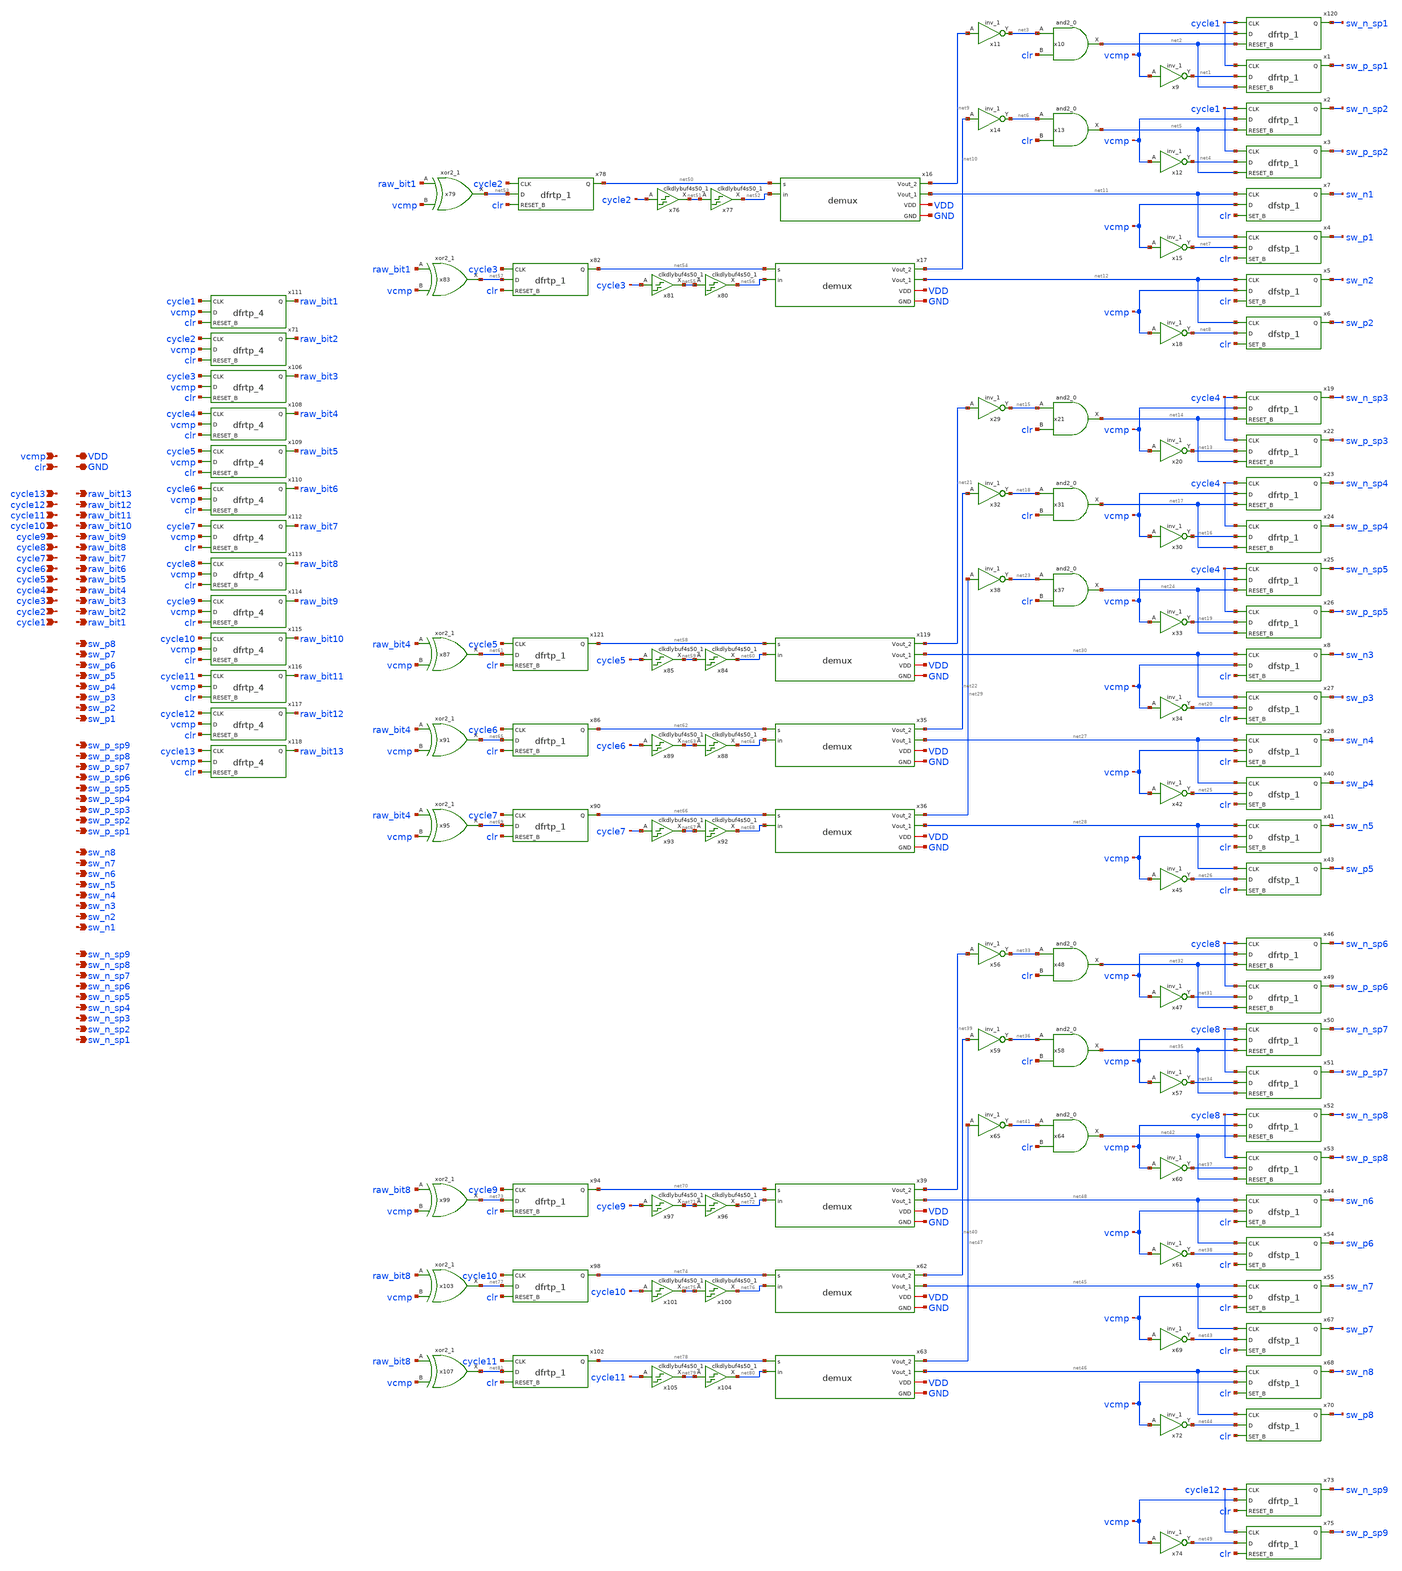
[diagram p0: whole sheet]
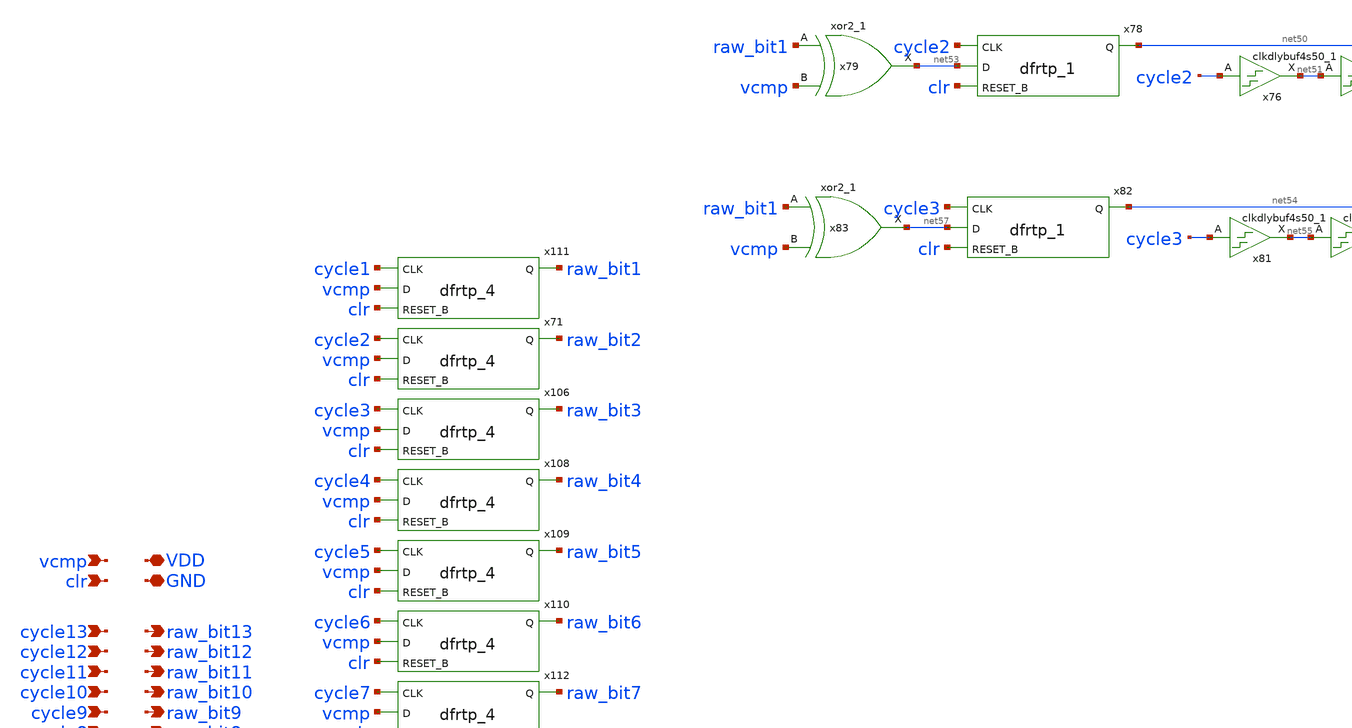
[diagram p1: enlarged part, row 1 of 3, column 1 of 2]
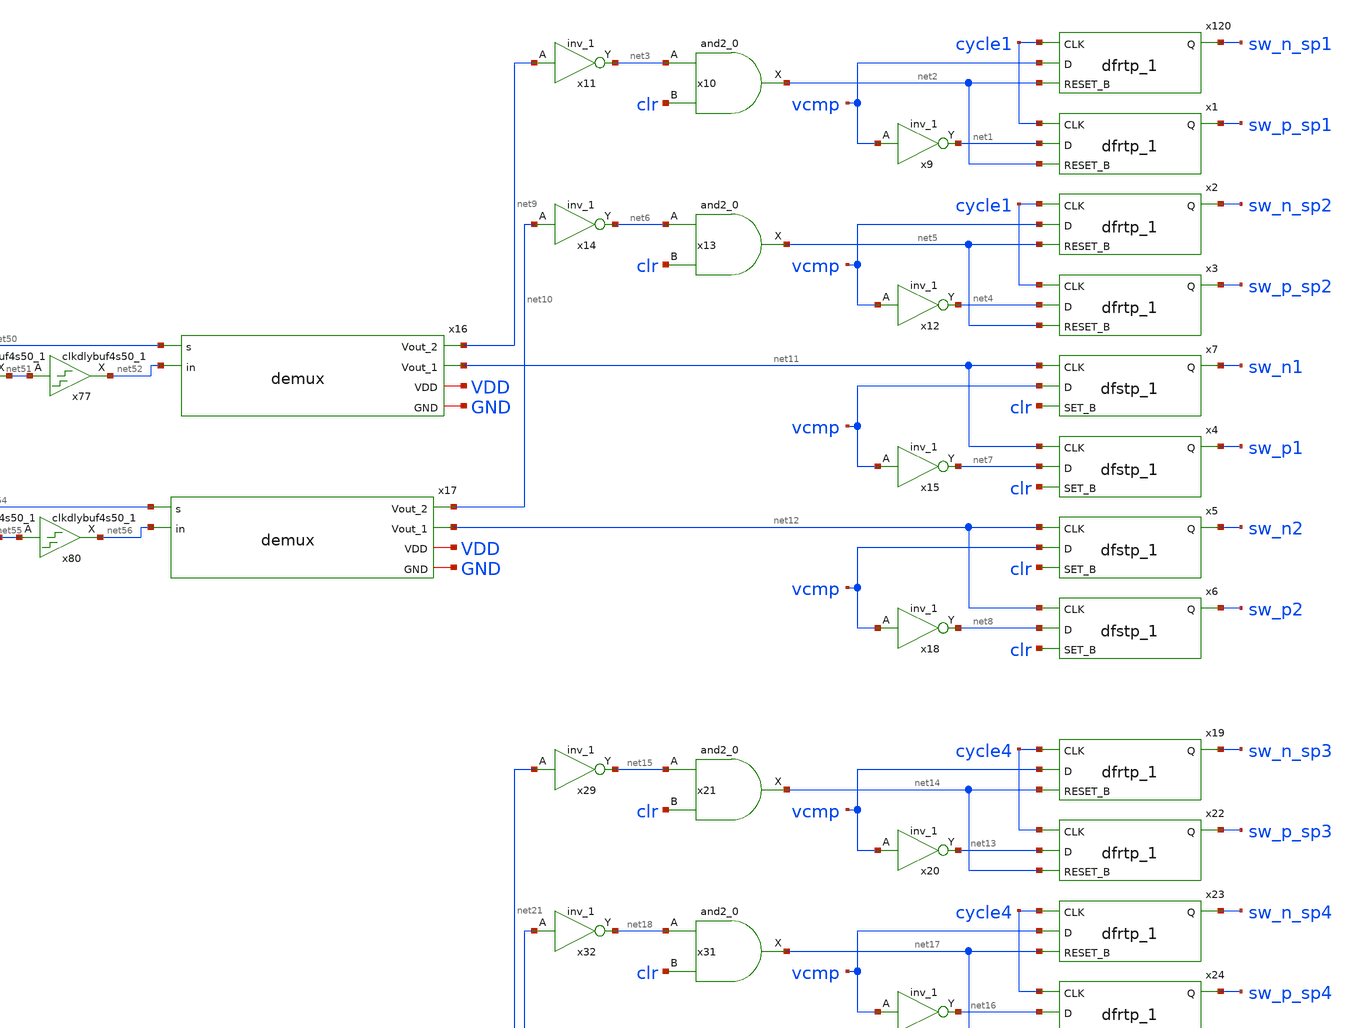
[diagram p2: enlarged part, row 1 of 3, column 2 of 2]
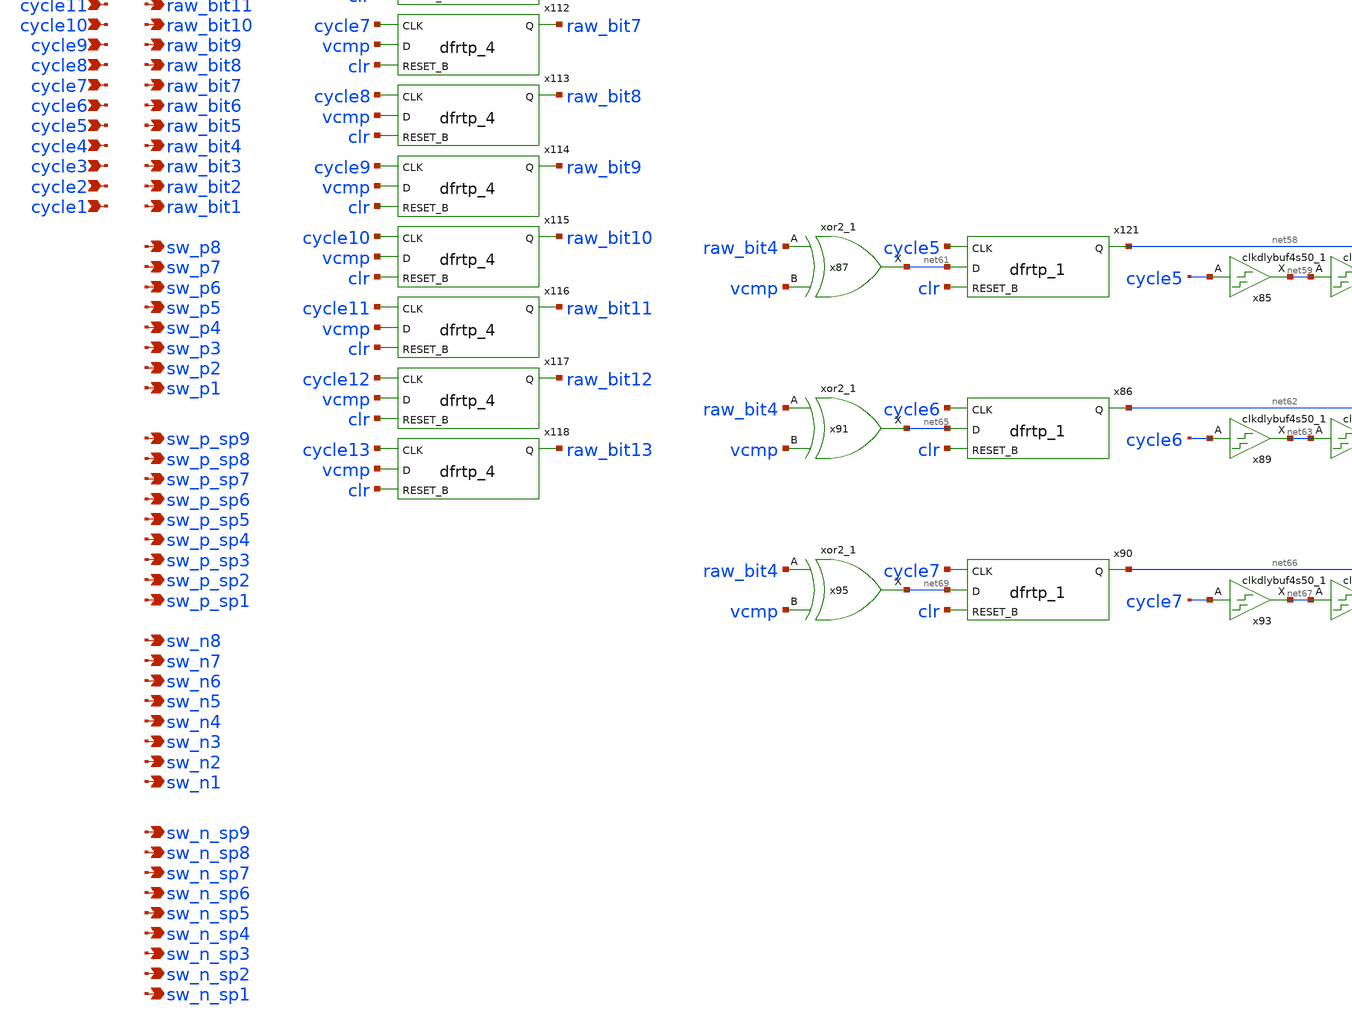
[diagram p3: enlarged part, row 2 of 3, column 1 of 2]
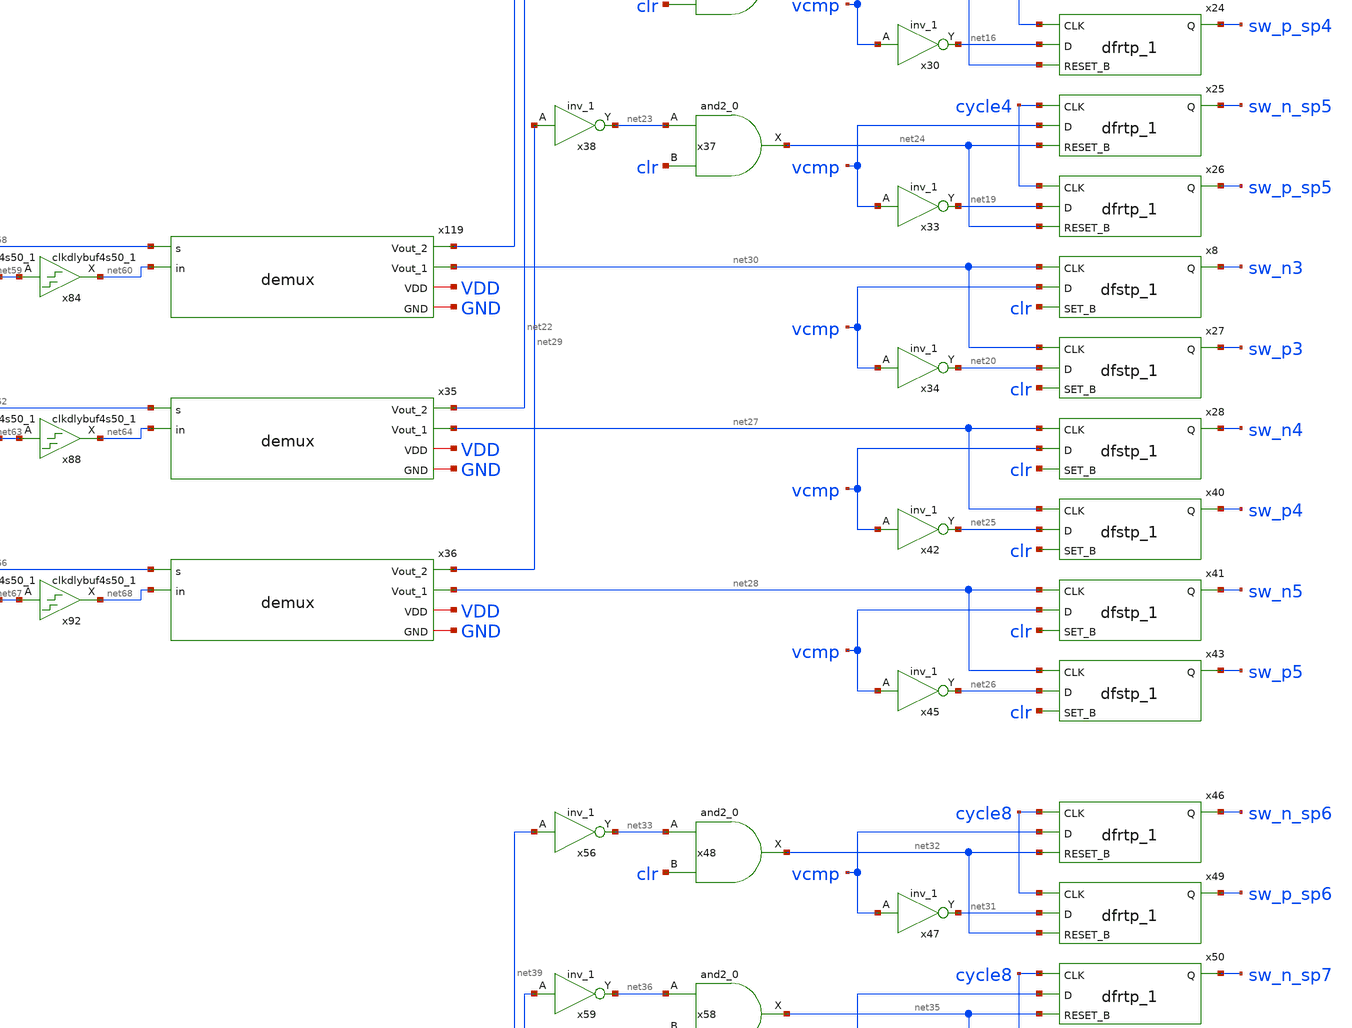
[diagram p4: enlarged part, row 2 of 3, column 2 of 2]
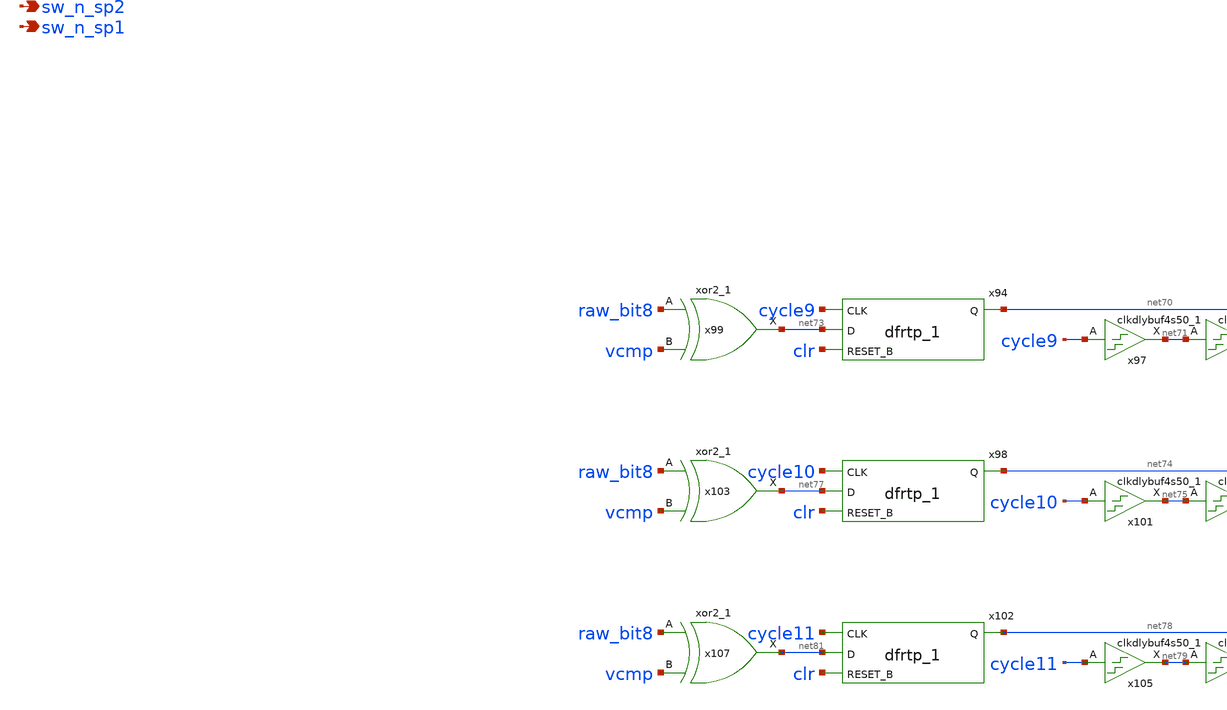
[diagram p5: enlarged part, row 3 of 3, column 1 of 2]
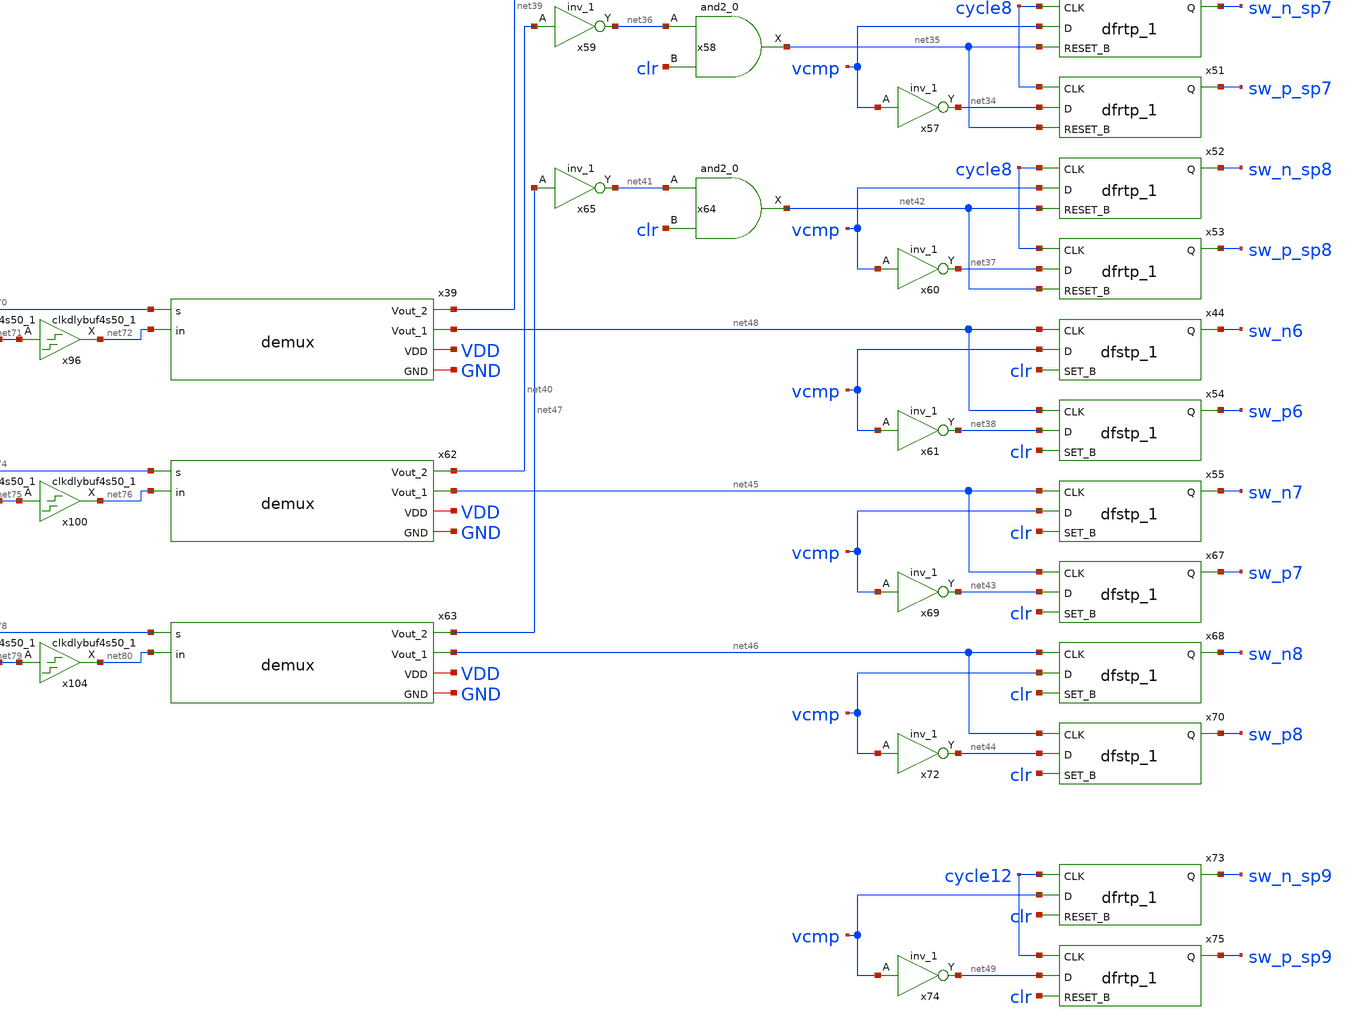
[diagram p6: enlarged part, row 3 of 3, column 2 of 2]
** sch_path: xschem/rawbitcalculator/rawbitcalc.sch
**.subckt rawbitcalc vcmp clr VDD GND cycle13 sw_p_sp8 sw_p8 raw_bit13 cycle12 cycle11 cycle10
*+ cycle9 cycle8 cycle7 cycle6 cycle5 cycle4 cycle3 cycle2 cycle1 raw_bit12 raw_bit11 raw_bit10 raw_bit9
*+ raw_bit8 raw_bit7 raw_bit6 raw_bit5 raw_bit4 raw_bit3 raw_bit2 raw_bit1 sw_p7 sw_p6 sw_p5 sw_p4 sw_p3 sw_p2
*+ sw_p1 sw_p_sp7 sw_p_sp6 sw_p_sp5 sw_p_sp4 sw_p_sp3 sw_p_sp2 sw_p_sp1 sw_p_sp9 sw_n_sp8 sw_n8 sw_n7 sw_n6
*+ sw_n5 sw_n4 sw_n3 sw_n2 sw_n1 sw_n_sp7 sw_n_sp6 sw_n_sp5 sw_n_sp4 sw_n_sp3 sw_n_sp2 sw_n_sp1 sw_n_sp9
*.ipin vcmp
*.ipin clr
*.iopin VDD
*.iopin GND
*.ipin cycle13
*.opin sw_p_sp8
*.opin sw_p8
*.opin raw_bit13
*.ipin cycle12
*.ipin cycle11
*.ipin cycle10
*.ipin cycle9
*.ipin cycle8
*.ipin cycle7
*.ipin cycle6
*.ipin cycle5
*.ipin cycle4
*.ipin cycle3
*.ipin cycle2
*.ipin cycle1
*.opin raw_bit12
*.opin raw_bit11
*.opin raw_bit10
*.opin raw_bit9
*.opin raw_bit8
*.opin raw_bit7
*.opin raw_bit6
*.opin raw_bit5
*.opin raw_bit4
*.opin raw_bit3
*.opin raw_bit2
*.opin raw_bit1
*.opin sw_p7
*.opin sw_p6
*.opin sw_p5
*.opin sw_p4
*.opin sw_p3
*.opin sw_p2
*.opin sw_p1
*.opin sw_p_sp7
*.opin sw_p_sp6
*.opin sw_p_sp5
*.opin sw_p_sp4
*.opin sw_p_sp3
*.opin sw_p_sp2
*.opin sw_p_sp1
*.opin sw_p_sp9
*.opin sw_n_sp8
*.opin sw_n8
*.opin sw_n7
*.opin sw_n6
*.opin sw_n5
*.opin sw_n4
*.opin sw_n3
*.opin sw_n2
*.opin sw_n1
*.opin sw_n_sp7
*.opin sw_n_sp6
*.opin sw_n_sp5
*.opin sw_n_sp4
*.opin sw_n_sp3
*.opin sw_n_sp2
*.opin sw_n_sp1
*.opin sw_n_sp9
x9 vcmp GND GND VDD VDD net1 sky130_fd_sc_hd__inv_1
x10 net3 clr GND GND VDD VDD net2 sky130_fd_sc_hd__and2_0
x11 net9 GND GND VDD VDD net3 sky130_fd_sc_hd__inv_1
x12 vcmp GND GND VDD VDD net4 sky130_fd_sc_hd__inv_1
x13 net6 clr GND GND VDD VDD net5 sky130_fd_sc_hd__and2_0
x14 net10 GND GND VDD VDD net6 sky130_fd_sc_hd__inv_1
x15 vcmp GND GND VDD VDD net7 sky130_fd_sc_hd__inv_1
x18 vcmp GND GND VDD VDD net8 sky130_fd_sc_hd__inv_1
x19 cycle4 vcmp net14 GND GND VDD VDD sw_n_sp3 sky130_fd_sc_hd__dfrtp_1
x20 vcmp GND GND VDD VDD net13 sky130_fd_sc_hd__inv_1
x21 net15 clr GND GND VDD VDD net14 sky130_fd_sc_hd__and2_0
x22 cycle4 net13 net14 GND GND VDD VDD sw_p_sp3 sky130_fd_sc_hd__dfrtp_1
x23 cycle4 vcmp net17 GND GND VDD VDD sw_n_sp4 sky130_fd_sc_hd__dfrtp_1
x24 cycle4 net16 net17 GND GND VDD VDD sw_p_sp4 sky130_fd_sc_hd__dfrtp_1
x25 cycle4 vcmp net24 GND GND VDD VDD sw_n_sp5 sky130_fd_sc_hd__dfrtp_1
x26 cycle4 net19 net24 GND GND VDD VDD sw_p_sp5 sky130_fd_sc_hd__dfrtp_1
x29 net21 GND GND VDD VDD net15 sky130_fd_sc_hd__inv_1
x30 vcmp GND GND VDD VDD net16 sky130_fd_sc_hd__inv_1
x31 net18 clr GND GND VDD VDD net17 sky130_fd_sc_hd__and2_0
x32 net22 GND GND VDD VDD net18 sky130_fd_sc_hd__inv_1
x33 vcmp GND GND VDD VDD net19 sky130_fd_sc_hd__inv_1
x34 vcmp GND GND VDD VDD net20 sky130_fd_sc_hd__inv_1
x37 net23 clr GND GND VDD VDD net24 sky130_fd_sc_hd__and2_0
x38 net29 GND GND VDD VDD net23 sky130_fd_sc_hd__inv_1
x42 vcmp GND GND VDD VDD net25 sky130_fd_sc_hd__inv_1
x45 vcmp GND GND VDD VDD net26 sky130_fd_sc_hd__inv_1
x46 cycle8 vcmp net32 GND GND VDD VDD sw_n_sp6 sky130_fd_sc_hd__dfrtp_1
x47 vcmp GND GND VDD VDD net31 sky130_fd_sc_hd__inv_1
x48 net33 clr GND GND VDD VDD net32 sky130_fd_sc_hd__and2_0
x49 cycle8 net31 net32 GND GND VDD VDD sw_p_sp6 sky130_fd_sc_hd__dfrtp_1
x50 cycle8 vcmp net35 GND GND VDD VDD sw_n_sp7 sky130_fd_sc_hd__dfrtp_1
x51 cycle8 net34 net35 GND GND VDD VDD sw_p_sp7 sky130_fd_sc_hd__dfrtp_1
x52 cycle8 vcmp net42 GND GND VDD VDD sw_n_sp8 sky130_fd_sc_hd__dfrtp_1
x53 cycle8 net37 net42 GND GND VDD VDD sw_p_sp8 sky130_fd_sc_hd__dfrtp_1
x56 net39 GND GND VDD VDD net33 sky130_fd_sc_hd__inv_1
x57 vcmp GND GND VDD VDD net34 sky130_fd_sc_hd__inv_1
x58 net36 clr GND GND VDD VDD net35 sky130_fd_sc_hd__and2_0
x59 net40 GND GND VDD VDD net36 sky130_fd_sc_hd__inv_1
x60 vcmp GND GND VDD VDD net37 sky130_fd_sc_hd__inv_1
x61 vcmp GND GND VDD VDD net38 sky130_fd_sc_hd__inv_1
x64 net41 clr GND GND VDD VDD net42 sky130_fd_sc_hd__and2_0
x65 net47 GND GND VDD VDD net41 sky130_fd_sc_hd__inv_1
x69 vcmp GND GND VDD VDD net43 sky130_fd_sc_hd__inv_1
x72 vcmp GND GND VDD VDD net44 sky130_fd_sc_hd__inv_1
x73 cycle12 vcmp clr GND GND VDD VDD sw_n_sp9 sky130_fd_sc_hd__dfrtp_1
x74 vcmp GND GND VDD VDD net49 sky130_fd_sc_hd__inv_1
x75 cycle12 net49 clr GND GND VDD VDD sw_p_sp9 sky130_fd_sc_hd__dfrtp_1
x77 net51 GND GND VDD VDD net52 sky130_fd_sc_hd__clkdlybuf4s50_1
x76 cycle2 GND GND VDD VDD net51 sky130_fd_sc_hd__clkdlybuf4s50_1
x78 cycle2 net53 clr GND GND VDD VDD net50 sky130_fd_sc_hd__dfrtp_1
x79 raw_bit1 vcmp GND GND VDD VDD net53 sky130_fd_sc_hd__xor2_1
x80 net55 GND GND VDD VDD net56 sky130_fd_sc_hd__clkdlybuf4s50_1
x81 cycle3 GND GND VDD VDD net55 sky130_fd_sc_hd__clkdlybuf4s50_1
x83 raw_bit1 vcmp GND GND VDD VDD net57 sky130_fd_sc_hd__xor2_1
x84 net59 GND GND VDD VDD net60 sky130_fd_sc_hd__clkdlybuf4s50_1
x85 cycle5 GND GND VDD VDD net59 sky130_fd_sc_hd__clkdlybuf4s50_1
x87 raw_bit4 vcmp GND GND VDD VDD net61 sky130_fd_sc_hd__xor2_1
x88 net63 GND GND VDD VDD net64 sky130_fd_sc_hd__clkdlybuf4s50_1
x89 cycle6 GND GND VDD VDD net63 sky130_fd_sc_hd__clkdlybuf4s50_1
x91 raw_bit4 vcmp GND GND VDD VDD net65 sky130_fd_sc_hd__xor2_1
x92 net67 GND GND VDD VDD net68 sky130_fd_sc_hd__clkdlybuf4s50_1
x93 cycle7 GND GND VDD VDD net67 sky130_fd_sc_hd__clkdlybuf4s50_1
x95 raw_bit4 vcmp GND GND VDD VDD net69 sky130_fd_sc_hd__xor2_1
x96 net71 GND GND VDD VDD net72 sky130_fd_sc_hd__clkdlybuf4s50_1
x97 cycle9 GND GND VDD VDD net71 sky130_fd_sc_hd__clkdlybuf4s50_1
x99 raw_bit8 vcmp GND GND VDD VDD net73 sky130_fd_sc_hd__xor2_1
x100 net75 GND GND VDD VDD net76 sky130_fd_sc_hd__clkdlybuf4s50_1
x101 cycle10 GND GND VDD VDD net75 sky130_fd_sc_hd__clkdlybuf4s50_1
x103 raw_bit8 vcmp GND GND VDD VDD net77 sky130_fd_sc_hd__xor2_1
x104 net79 GND GND VDD VDD net80 sky130_fd_sc_hd__clkdlybuf4s50_1
x105 cycle11 GND GND VDD VDD net79 sky130_fd_sc_hd__clkdlybuf4s50_1
x107 raw_bit8 vcmp GND GND VDD VDD net81 sky130_fd_sc_hd__xor2_1
x82 cycle3 net57 clr GND GND VDD VDD net54 sky130_fd_sc_hd__dfrtp_1
x121 cycle5 net61 clr GND GND VDD VDD net58 sky130_fd_sc_hd__dfrtp_1
x86 cycle6 net65 clr GND GND VDD VDD net62 sky130_fd_sc_hd__dfrtp_1
x90 cycle7 net69 clr GND GND VDD VDD net66 sky130_fd_sc_hd__dfrtp_1
x94 cycle9 net73 clr GND GND VDD VDD net70 sky130_fd_sc_hd__dfrtp_1
x98 cycle10 net77 clr GND GND VDD VDD net74 sky130_fd_sc_hd__dfrtp_1
x102 cycle11 net81 clr GND GND VDD VDD net78 sky130_fd_sc_hd__dfrtp_1
x120 cycle1 vcmp net2 GND GND VDD VDD sw_n_sp1 sky130_fd_sc_hd__dfrtp_1
x1 cycle1 net1 net2 GND GND VDD VDD sw_p_sp1 sky130_fd_sc_hd__dfrtp_1
x2 cycle1 vcmp net5 GND GND VDD VDD sw_n_sp2 sky130_fd_sc_hd__dfrtp_1
x3 cycle1 net4 net5 GND GND VDD VDD sw_p_sp2 sky130_fd_sc_hd__dfrtp_1
x7 net11 vcmp clr GND GND VDD VDD sw_n1 sky130_fd_sc_hd__dfstp_1
x4 net11 net7 clr GND GND VDD VDD sw_p1 sky130_fd_sc_hd__dfstp_1
x5 net12 vcmp clr GND GND VDD VDD sw_n2 sky130_fd_sc_hd__dfstp_1
x6 net12 net8 clr GND GND VDD VDD sw_p2 sky130_fd_sc_hd__dfstp_1
x8 net30 vcmp clr GND GND VDD VDD sw_n3 sky130_fd_sc_hd__dfstp_1
x27 net30 net20 clr GND GND VDD VDD sw_p3 sky130_fd_sc_hd__dfstp_1
x28 net27 vcmp clr GND GND VDD VDD sw_n4 sky130_fd_sc_hd__dfstp_1
x40 net27 net25 clr GND GND VDD VDD sw_p4 sky130_fd_sc_hd__dfstp_1
x41 net28 vcmp clr GND GND VDD VDD sw_n5 sky130_fd_sc_hd__dfstp_1
x43 net28 net26 clr GND GND VDD VDD sw_p5 sky130_fd_sc_hd__dfstp_1
x44 net48 vcmp clr GND GND VDD VDD sw_n6 sky130_fd_sc_hd__dfstp_1
x54 net48 net38 clr GND GND VDD VDD sw_p6 sky130_fd_sc_hd__dfstp_1
x55 net45 vcmp clr GND GND VDD VDD sw_n7 sky130_fd_sc_hd__dfstp_1
x67 net45 net43 clr GND GND VDD VDD sw_p7 sky130_fd_sc_hd__dfstp_1
x68 net46 vcmp clr GND GND VDD VDD sw_n8 sky130_fd_sc_hd__dfstp_1
x70 net46 net44 clr GND GND VDD VDD sw_p8 sky130_fd_sc_hd__dfstp_1
x111 cycle1 vcmp clr GND GND VDD VDD raw_bit1 sky130_fd_sc_hd__dfrtp_4
x71 cycle2 vcmp clr GND GND VDD VDD raw_bit2 sky130_fd_sc_hd__dfrtp_4
x106 cycle3 vcmp clr GND GND VDD VDD raw_bit3 sky130_fd_sc_hd__dfrtp_4
x108 cycle4 vcmp clr GND GND VDD VDD raw_bit4 sky130_fd_sc_hd__dfrtp_4
x109 cycle5 vcmp clr GND GND VDD VDD raw_bit5 sky130_fd_sc_hd__dfrtp_4
x110 cycle6 vcmp clr GND GND VDD VDD raw_bit6 sky130_fd_sc_hd__dfrtp_4
x112 cycle7 vcmp clr GND GND VDD VDD raw_bit7 sky130_fd_sc_hd__dfrtp_4
x113 cycle8 vcmp clr GND GND VDD VDD raw_bit8 sky130_fd_sc_hd__dfrtp_4
x114 cycle9 vcmp clr GND GND VDD VDD raw_bit9 sky130_fd_sc_hd__dfrtp_4
x115 cycle10 vcmp clr GND GND VDD VDD raw_bit10 sky130_fd_sc_hd__dfrtp_4
x116 cycle11 vcmp clr GND GND VDD VDD raw_bit11 sky130_fd_sc_hd__dfrtp_4
x117 cycle12 vcmp clr GND GND VDD VDD raw_bit12 sky130_fd_sc_hd__dfrtp_4
x118 cycle13 vcmp clr GND GND VDD VDD raw_bit13 sky130_fd_sc_hd__dfrtp_4
x16 net50 net11 net52 VDD GND net9 demux
x17 net54 net12 net56 VDD GND net10 demux
x119 net58 net30 net60 VDD GND net21 demux
x35 net62 net27 net64 VDD GND net22 demux
x36 net66 net28 net68 VDD GND net29 demux
x39 net70 net48 net72 VDD GND net39 demux
x62 net74 net45 net76 VDD GND net40 demux
x63 net78 net46 net80 VDD GND net47 demux
**.ends
.end
